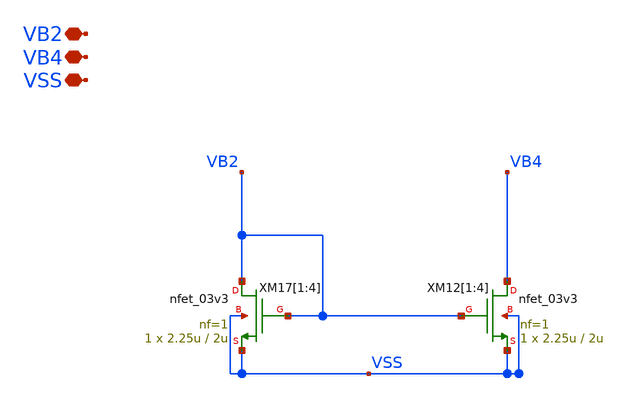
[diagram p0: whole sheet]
** sch_path: TIA_Filter/Folded/FC_bias_nfets.sch
**.subckt FC_bias_nfets VB4 VB2 VSS
*.iopin VB4
*.iopin VB2
*.iopin VSS
XM17[1] VB2 VB2 VSS VSS nfet_03v3 L=2u W=2.25u nf=1 ad='int((nf+1)/2) * W/nf * 0.18u' as='int((nf+2)/2) * W/nf * 0.18u'
+ pd='2*int((nf+1)/2) * (W/nf + 0.18u)' ps='2*int((nf+2)/2) * (W/nf + 0.18u)' nrd='0.18u / W' nrs='0.18u / W'
+ sa=0 sb=0 sd=0 m=1
XM17[2] VB2 VB2 VSS VSS nfet_03v3 L=2u W=2.25u nf=1 ad='int((nf+1)/2) * W/nf * 0.18u' as='int((nf+2)/2) * W/nf * 0.18u'
+ pd='2*int((nf+1)/2) * (W/nf + 0.18u)' ps='2*int((nf+2)/2) * (W/nf + 0.18u)' nrd='0.18u / W' nrs='0.18u / W'
+ sa=0 sb=0 sd=0 m=1
XM17[3] VB2 VB2 VSS VSS nfet_03v3 L=2u W=2.25u nf=1 ad='int((nf+1)/2) * W/nf * 0.18u' as='int((nf+2)/2) * W/nf * 0.18u'
+ pd='2*int((nf+1)/2) * (W/nf + 0.18u)' ps='2*int((nf+2)/2) * (W/nf + 0.18u)' nrd='0.18u / W' nrs='0.18u / W'
+ sa=0 sb=0 sd=0 m=1
XM17[4] VB2 VB2 VSS VSS nfet_03v3 L=2u W=2.25u nf=1 ad='int((nf+1)/2) * W/nf * 0.18u' as='int((nf+2)/2) * W/nf * 0.18u'
+ pd='2*int((nf+1)/2) * (W/nf + 0.18u)' ps='2*int((nf+2)/2) * (W/nf + 0.18u)' nrd='0.18u / W' nrs='0.18u / W'
+ sa=0 sb=0 sd=0 m=1
XM12[1] VB4 VB2 VSS VSS nfet_03v3 L=2u W=2.25u nf=1 ad='int((nf+1)/2) * W/nf * 0.18u' as='int((nf+2)/2) * W/nf * 0.18u'
+ pd='2*int((nf+1)/2) * (W/nf + 0.18u)' ps='2*int((nf+2)/2) * (W/nf + 0.18u)' nrd='0.18u / W' nrs='0.18u / W'
+ sa=0 sb=0 sd=0 m=1
XM12[2] VB4 VB2 VSS VSS nfet_03v3 L=2u W=2.25u nf=1 ad='int((nf+1)/2) * W/nf * 0.18u' as='int((nf+2)/2) * W/nf * 0.18u'
+ pd='2*int((nf+1)/2) * (W/nf + 0.18u)' ps='2*int((nf+2)/2) * (W/nf + 0.18u)' nrd='0.18u / W' nrs='0.18u / W'
+ sa=0 sb=0 sd=0 m=1
XM12[3] VB4 VB2 VSS VSS nfet_03v3 L=2u W=2.25u nf=1 ad='int((nf+1)/2) * W/nf * 0.18u' as='int((nf+2)/2) * W/nf * 0.18u'
+ pd='2*int((nf+1)/2) * (W/nf + 0.18u)' ps='2*int((nf+2)/2) * (W/nf + 0.18u)' nrd='0.18u / W' nrs='0.18u / W'
+ sa=0 sb=0 sd=0 m=1
XM12[4] VB4 VB2 VSS VSS nfet_03v3 L=2u W=2.25u nf=1 ad='int((nf+1)/2) * W/nf * 0.18u' as='int((nf+2)/2) * W/nf * 0.18u'
+ pd='2*int((nf+1)/2) * (W/nf + 0.18u)' ps='2*int((nf+2)/2) * (W/nf + 0.18u)' nrd='0.18u / W' nrs='0.18u / W'
+ sa=0 sb=0 sd=0 m=1
**.ends
.end
